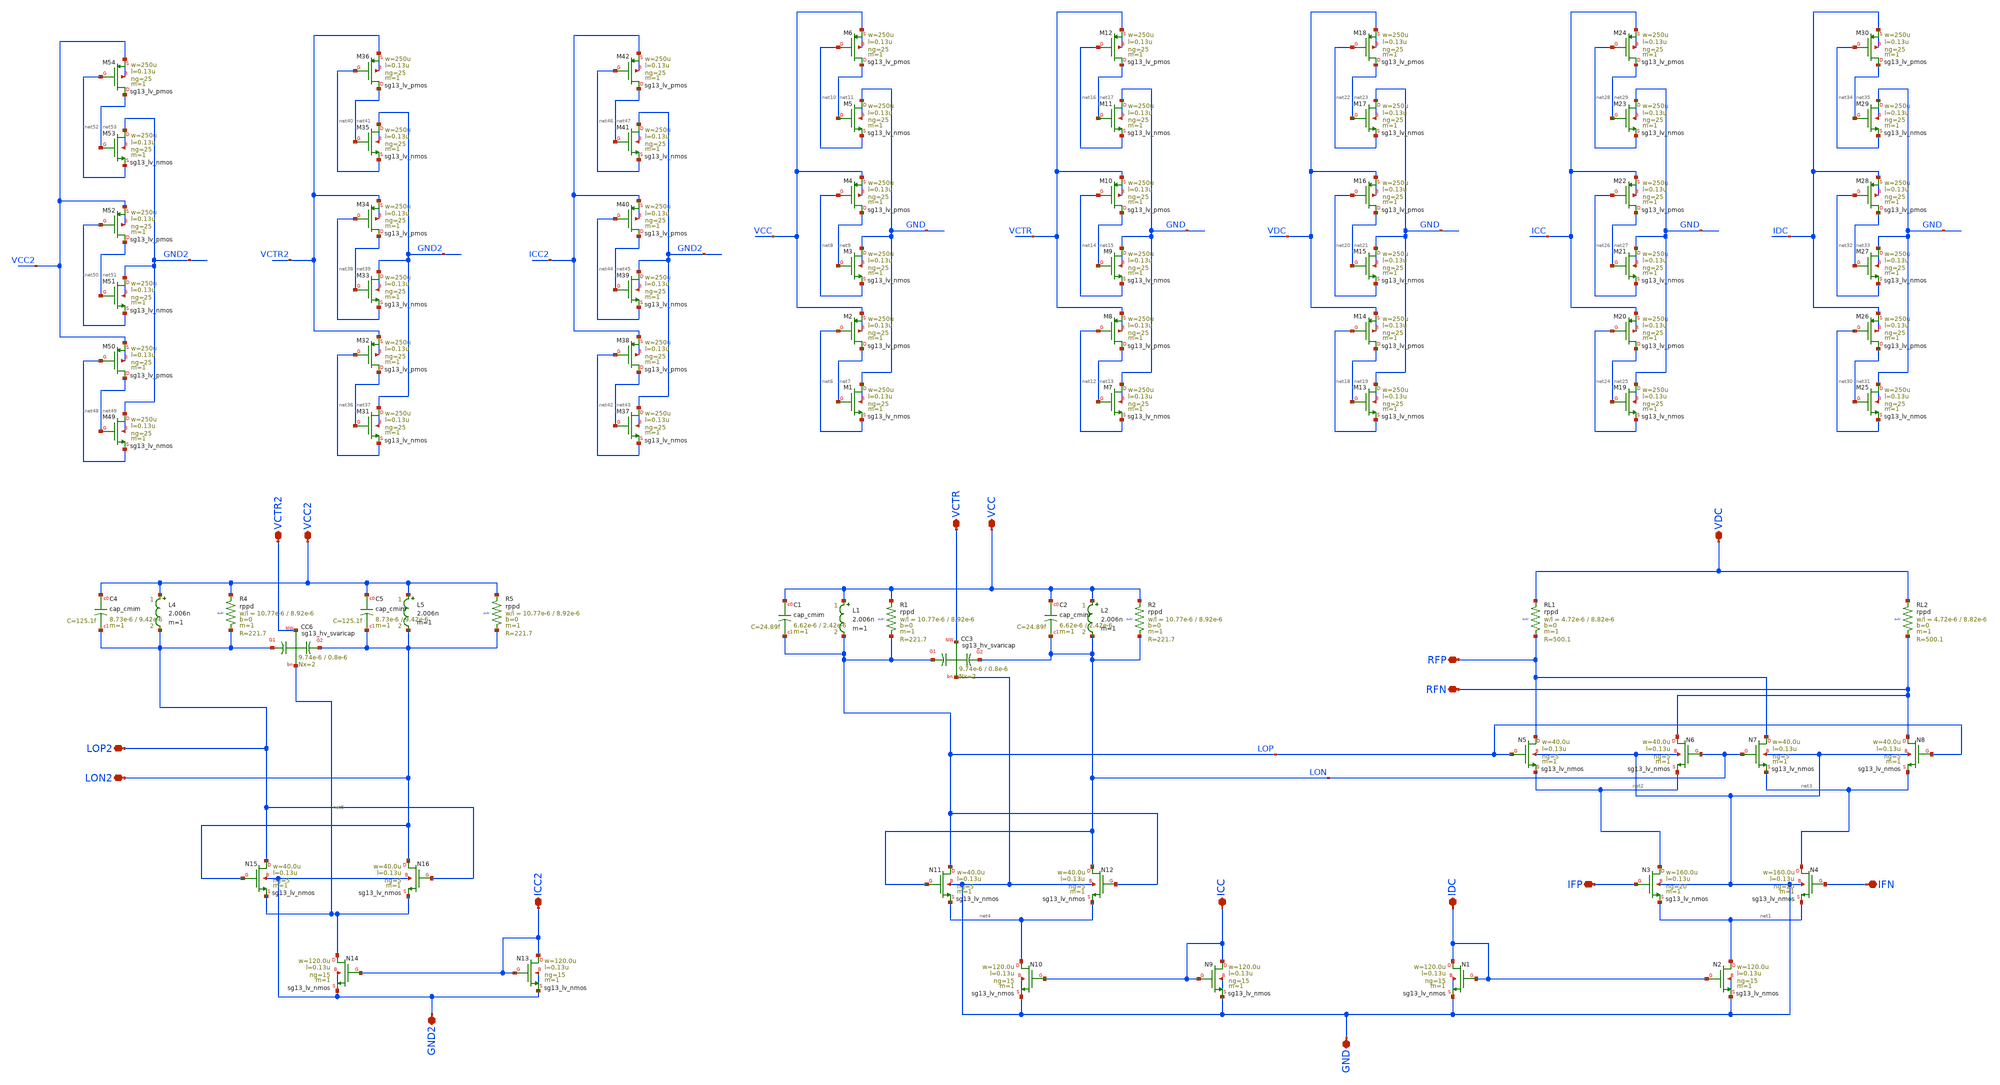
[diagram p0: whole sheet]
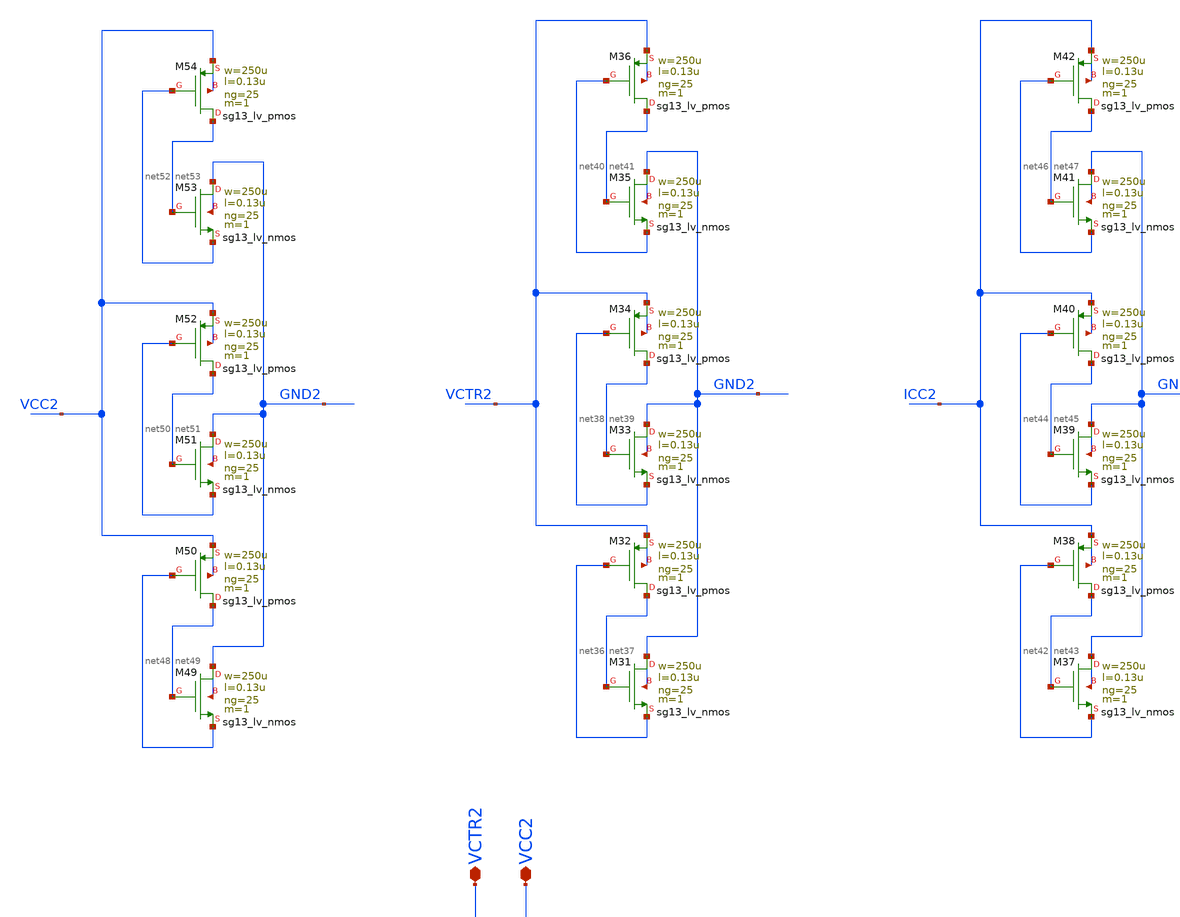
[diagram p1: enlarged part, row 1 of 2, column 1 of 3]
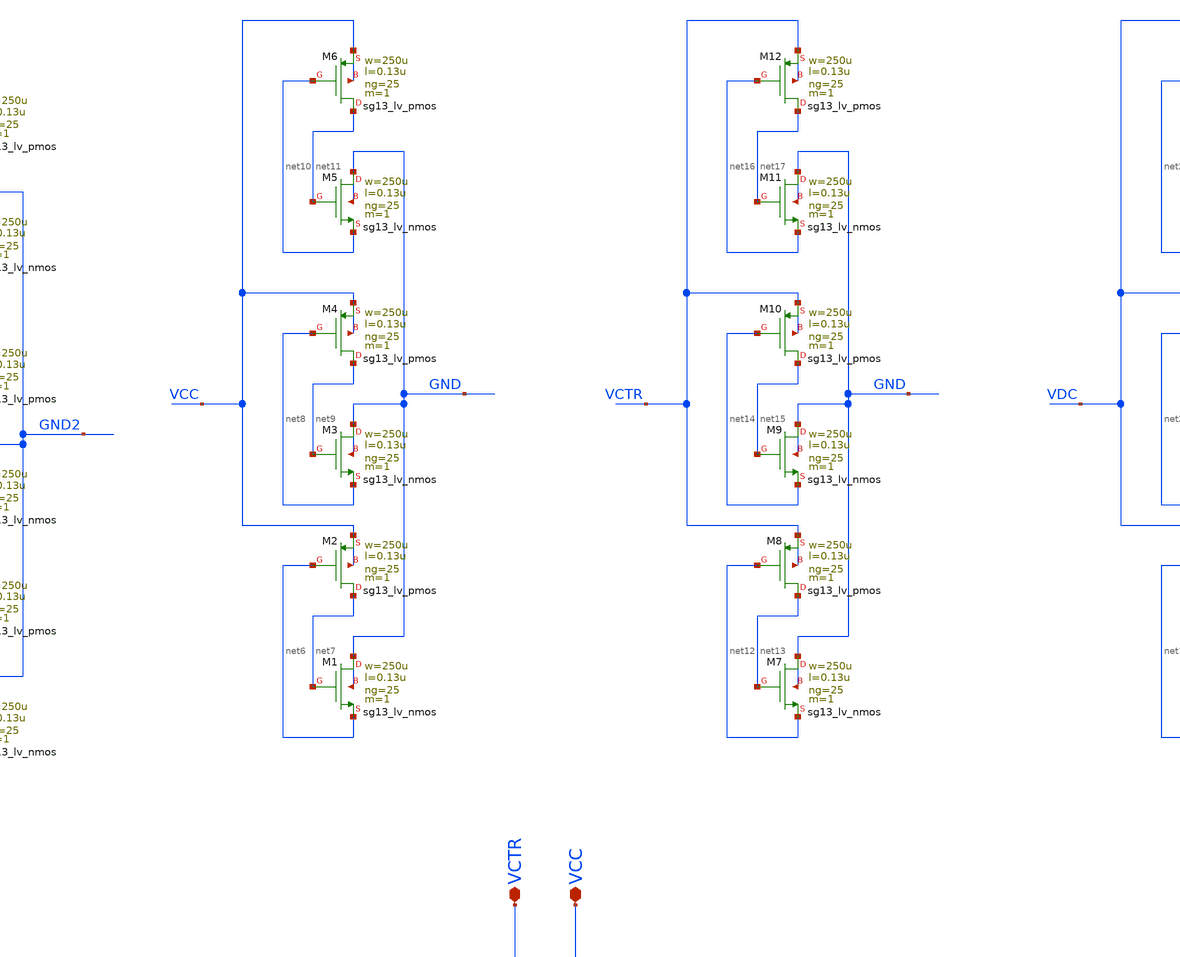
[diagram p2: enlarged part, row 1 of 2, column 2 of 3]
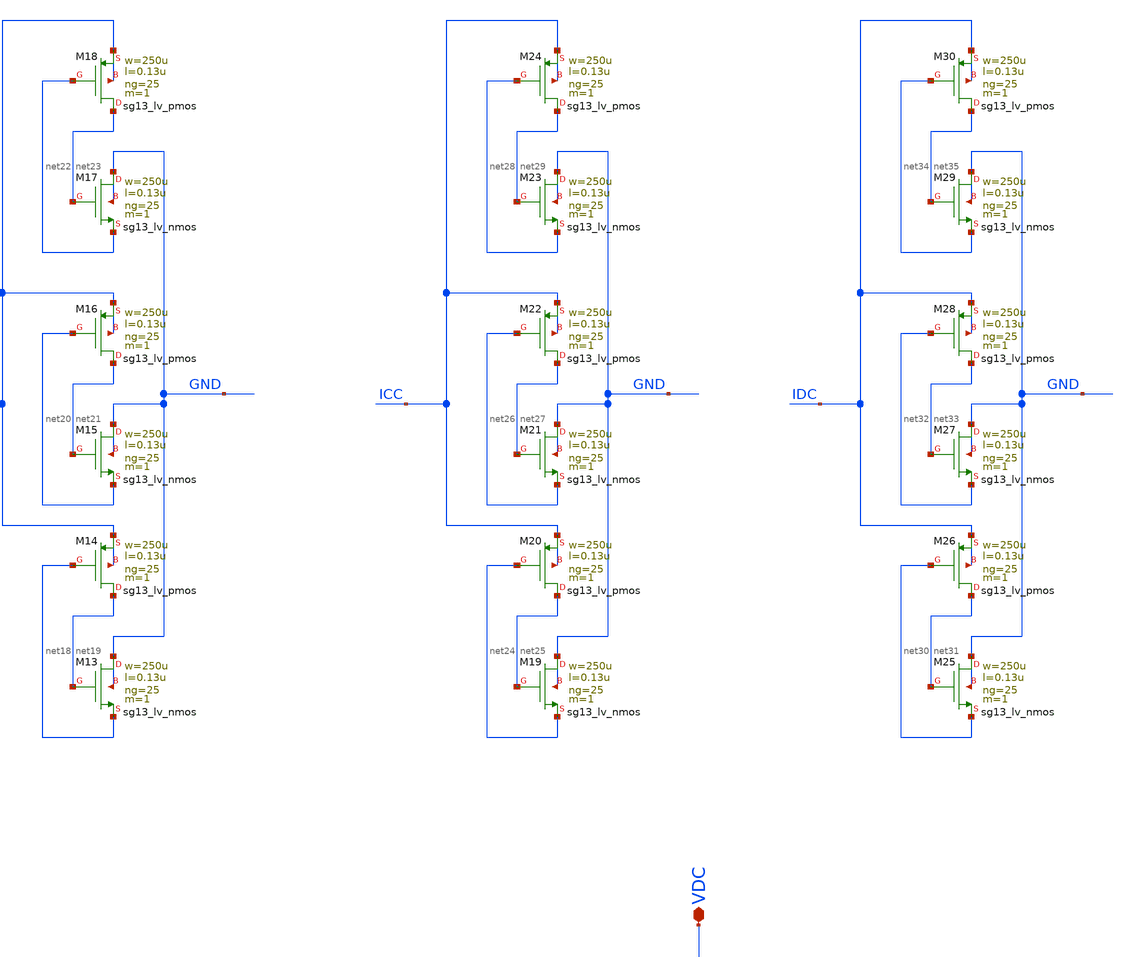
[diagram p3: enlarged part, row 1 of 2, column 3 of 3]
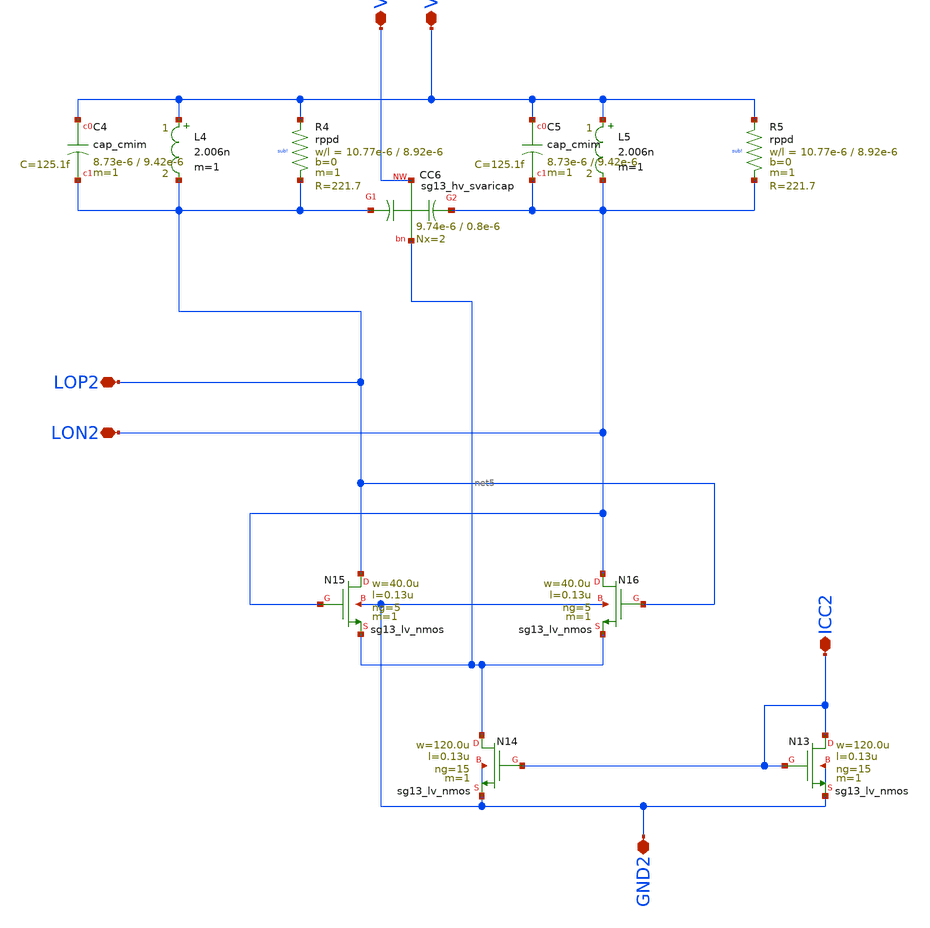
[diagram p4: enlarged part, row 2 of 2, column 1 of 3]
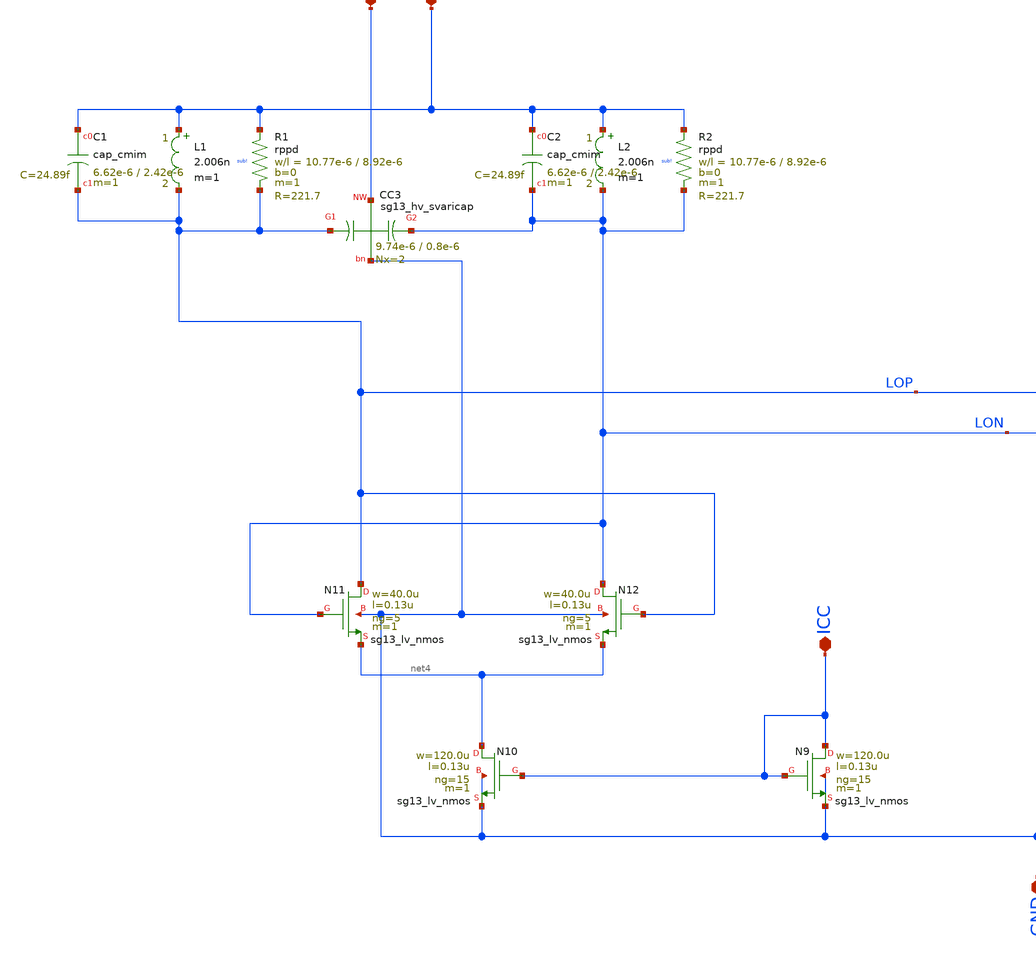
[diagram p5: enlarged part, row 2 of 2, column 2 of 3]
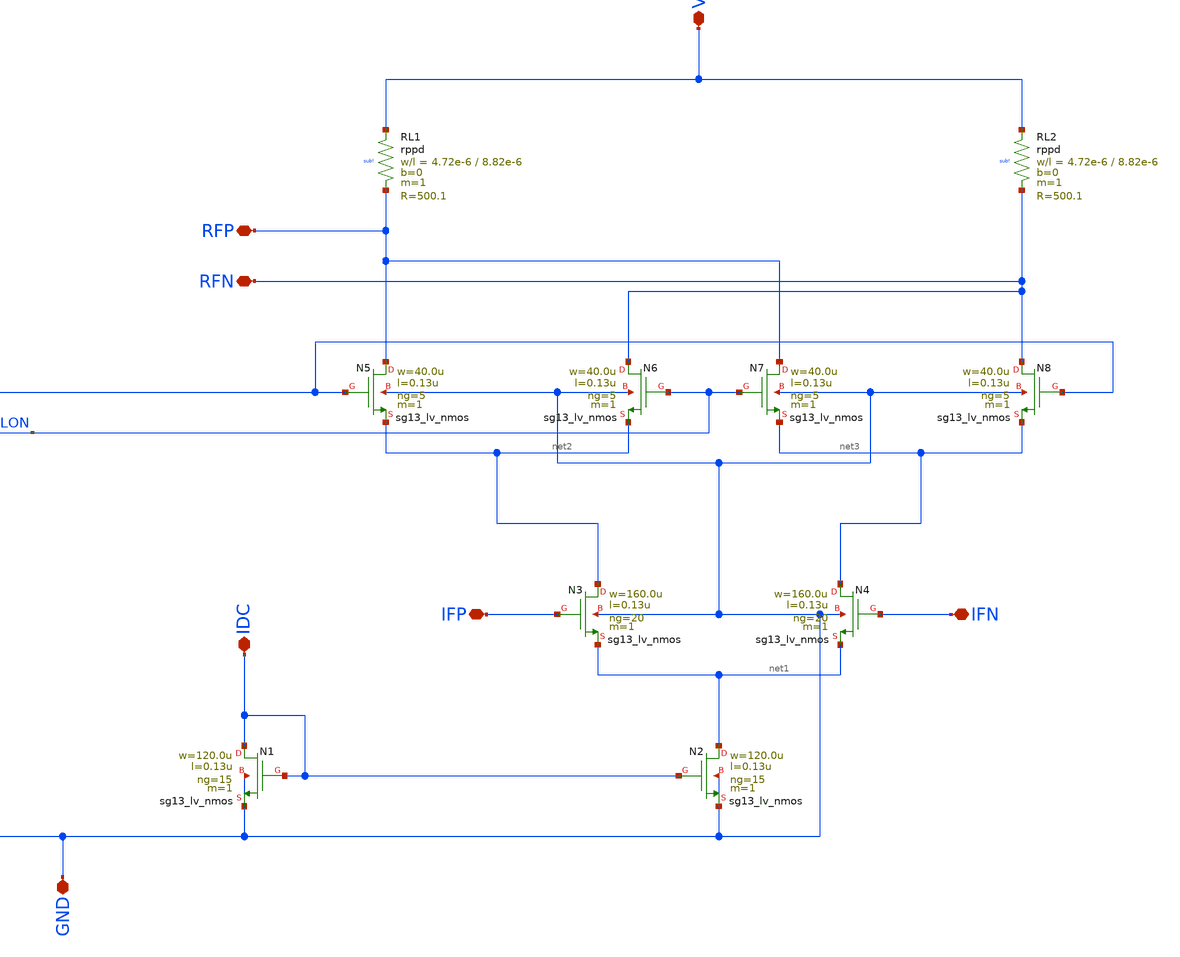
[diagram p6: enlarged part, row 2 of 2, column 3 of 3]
** sch_path: Up_Converter_5GHz/design_data/xschem/FMD_QNC_Up_Converter_5GHz.sch
**.subckt FMD_QNC_Up_Converter_5GHz RFN RFP VDC IFP IFN GND ICC LON2 LOP2 VCC2 ICC2 GND2 IDC VCTR2
*+ VCTR VCC
*.iopin RFN
*.iopin RFP
*.iopin VDC
*.iopin IFP
*.iopin IFN
*.iopin GND
*.iopin ICC
*.iopin LON2
*.iopin LOP2
*.iopin VCC2
*.iopin ICC2
*.iopin GND2
*.iopin IDC
*.iopin VCTR2
*.iopin VCTR
*.iopin VCC
XN6 RFN LON net2 GND sg13_lv_nmos w=40.0u l=0.13u ng=5 m=1 mm_ok=1
XRL2 VDC RFN sub! rppd w=4.72e-6 l=8.82e-6 m=1 b=0 mm_ok=1
XRL1 VDC RFP sub! rppd w=4.72e-6 l=8.82e-6 m=1 b=0 mm_ok=1
XN8 RFN LOP net3 GND sg13_lv_nmos w=40.0u l=0.13u ng=5 m=1 mm_ok=1
XN7 RFP LON net3 GND sg13_lv_nmos w=40.0u l=0.13u ng=5 m=1 mm_ok=1
XN5 RFP LOP net2 GND sg13_lv_nmos w=40.0u l=0.13u ng=5 m=1 mm_ok=1
XN4 net3 IFN net1 GND sg13_lv_nmos w=160.0u l=0.13u ng=20 m=1 mm_ok=1
XN3 net2 IFP net1 GND sg13_lv_nmos w=160.0u l=0.13u ng=20 m=1 mm_ok=1
XN1 IDC IDC GND GND sg13_lv_nmos w=120.0u l=0.13u ng=15 m=1 mm_ok=1
XN2 net1 IDC GND GND sg13_lv_nmos w=120.0u l=0.13u ng=15 m=1 mm_ok=1
XN11 LOP LON net4 GND sg13_lv_nmos w=40.0u l=0.13u ng=5 m=1 mm_ok=1
XN12 LON LOP net4 GND sg13_lv_nmos w=40.0u l=0.13u ng=5 m=1 mm_ok=1
XN9 ICC ICC GND GND sg13_lv_nmos w=120.0u l=0.13u ng=15 m=1 mm_ok=1
XN10 net4 ICC GND GND sg13_lv_nmos w=120.0u l=0.13u ng=15 m=1 mm_ok=1
XC1 VCC LOP cap_cmim w=6.62e-6 l=2.42e-6 m=1 mm_ok=1
XR1 VCC LOP sub! rppd w=10.77e-6 l=8.92e-6 m=1 b=0 mm_ok=1
XC2 VCC LON cap_cmim w=6.62e-6 l=2.42e-6 m=1 mm_ok=1
XR2 VCC LON sub! rppd w=10.77e-6 l=8.92e-6 m=1 b=0 mm_ok=1
XN15 LOP2 LON2 net5 GND2 sg13_lv_nmos w=40.0u l=0.13u ng=5 m=1 mm_ok=1
XN16 LON2 LOP2 net5 GND2 sg13_lv_nmos w=40.0u l=0.13u ng=5 m=1 mm_ok=1
XN13 ICC2 ICC2 GND2 GND2 sg13_lv_nmos w=120.0u l=0.13u ng=15 m=1 mm_ok=1
XN14 net5 ICC2 GND2 GND2 sg13_lv_nmos w=120.0u l=0.13u ng=15 m=1 mm_ok=1
XC4 VCC2 LOP2 cap_cmim w=8.73e-6 l=9.42e-6 m=1 mm_ok=1
XR4 VCC2 LOP2 sub! rppd w=10.77e-6 l=8.92e-6 m=1 b=0 mm_ok=1
XC5 VCC2 LON2 cap_cmim w=8.73e-6 l=9.42e-6 m=1 mm_ok=1
XR5 VCC2 LON2 sub! rppd w=10.77e-6 l=8.92e-6 m=1 b=0 mm_ok=1
L4 VCC2 LOP2 2.006n m=1
L1 VCC LOP 2.006n m=1
L2 VCC LON 2.006n m=1
L5 VCC2 LON2 2.006n m=1
XC6 LOP2 VCTR2 LON2 net5 sg13_hv_svaricap w=9.74e-6 l=0.8e-6 Nx=2
XC3 LOP VCTR LON GND sg13_hv_svaricap w=9.74e-6 l=0.8e-6 Nx=2
XM1 GND net7 net6 GND sg13_lv_nmos w=250u l=0.13u ng=25 m=1 mm_ok=1
XM2 net7 net6 VCC VCC sg13_lv_pmos w=250u l=0.13u ng=25 m=1 mm_ok=1
XM3 GND net9 net8 GND sg13_lv_nmos w=250u l=0.13u ng=25 m=1 mm_ok=1
XM4 net9 net8 VCC VCC sg13_lv_pmos w=250u l=0.13u ng=25 m=1 mm_ok=1
XM5 GND net11 net10 GND sg13_lv_nmos w=250u l=0.13u ng=25 m=1 mm_ok=1
XM6 net11 net10 VCC VCC sg13_lv_pmos w=250u l=0.13u ng=25 m=1 mm_ok=1
XM7 GND net13 net12 GND sg13_lv_nmos w=250u l=0.13u ng=25 m=1 mm_ok=1
XM8 net13 net12 VCTR VCTR sg13_lv_pmos w=250u l=0.13u ng=25 m=1 mm_ok=1
XM9 GND net15 net14 GND sg13_lv_nmos w=250u l=0.13u ng=25 m=1 mm_ok=1
XM10 net15 net14 VCTR VCTR sg13_lv_pmos w=250u l=0.13u ng=25 m=1 mm_ok=1
XM11 GND net17 net16 GND sg13_lv_nmos w=250u l=0.13u ng=25 m=1 mm_ok=1
XM12 net17 net16 VCTR VCTR sg13_lv_pmos w=250u l=0.13u ng=25 m=1 mm_ok=1
XM13 GND net19 net18 GND sg13_lv_nmos w=250u l=0.13u ng=25 m=1 mm_ok=1
XM14 net19 net18 VDC VDC sg13_lv_pmos w=250u l=0.13u ng=25 m=1 mm_ok=1
XM15 GND net21 net20 GND sg13_lv_nmos w=250u l=0.13u ng=25 m=1 mm_ok=1
XM16 net21 net20 VDC VDC sg13_lv_pmos w=250u l=0.13u ng=25 m=1 mm_ok=1
XM17 GND net23 net22 GND sg13_lv_nmos w=250u l=0.13u ng=25 m=1 mm_ok=1
XM18 net23 net22 VDC VDC sg13_lv_pmos w=250u l=0.13u ng=25 m=1 mm_ok=1
XM19 GND net25 net24 GND sg13_lv_nmos w=250u l=0.13u ng=25 m=1 mm_ok=1
XM20 net25 net24 ICC ICC sg13_lv_pmos w=250u l=0.13u ng=25 m=1 mm_ok=1
XM21 GND net27 net26 GND sg13_lv_nmos w=250u l=0.13u ng=25 m=1 mm_ok=1
XM22 net27 net26 ICC ICC sg13_lv_pmos w=250u l=0.13u ng=25 m=1 mm_ok=1
XM23 GND net29 net28 GND sg13_lv_nmos w=250u l=0.13u ng=25 m=1 mm_ok=1
XM24 net29 net28 ICC ICC sg13_lv_pmos w=250u l=0.13u ng=25 m=1 mm_ok=1
XM25 GND net31 net30 GND sg13_lv_nmos w=250u l=0.13u ng=25 m=1 mm_ok=1
XM26 net31 net30 IDC IDC sg13_lv_pmos w=250u l=0.13u ng=25 m=1 mm_ok=1
XM27 GND net33 net32 GND sg13_lv_nmos w=250u l=0.13u ng=25 m=1 mm_ok=1
XM28 net33 net32 IDC IDC sg13_lv_pmos w=250u l=0.13u ng=25 m=1 mm_ok=1
XM29 GND net35 net34 GND sg13_lv_nmos w=250u l=0.13u ng=25 m=1 mm_ok=1
XM30 net35 net34 IDC IDC sg13_lv_pmos w=250u l=0.13u ng=25 m=1 mm_ok=1
XM31 GND2 net37 net36 GND2 sg13_lv_nmos w=250u l=0.13u ng=25 m=1 mm_ok=1
XM32 net37 net36 VCTR2 VCTR2 sg13_lv_pmos w=250u l=0.13u ng=25 m=1 mm_ok=1
XM33 GND2 net39 net38 GND2 sg13_lv_nmos w=250u l=0.13u ng=25 m=1 mm_ok=1
XM34 net39 net38 VCTR2 VCTR2 sg13_lv_pmos w=250u l=0.13u ng=25 m=1 mm_ok=1
XM35 GND2 net41 net40 GND2 sg13_lv_nmos w=250u l=0.13u ng=25 m=1 mm_ok=1
XM36 net41 net40 VCTR2 VCTR2 sg13_lv_pmos w=250u l=0.13u ng=25 m=1 mm_ok=1
XM37 GND2 net43 net42 GND2 sg13_lv_nmos w=250u l=0.13u ng=25 m=1 mm_ok=1
XM38 net43 net42 ICC2 ICC2 sg13_lv_pmos w=250u l=0.13u ng=25 m=1 mm_ok=1
XM39 GND2 net45 net44 GND2 sg13_lv_nmos w=250u l=0.13u ng=25 m=1 mm_ok=1
XM40 net45 net44 ICC2 ICC2 sg13_lv_pmos w=250u l=0.13u ng=25 m=1 mm_ok=1
XM41 GND2 net47 net46 GND2 sg13_lv_nmos w=250u l=0.13u ng=25 m=1 mm_ok=1
XM42 net47 net46 ICC2 ICC2 sg13_lv_pmos w=250u l=0.13u ng=25 m=1 mm_ok=1
XM49 GND2 net49 net48 GND2 sg13_lv_nmos w=250u l=0.13u ng=25 m=1 mm_ok=1
XM50 net49 net48 VCC2 VCC2 sg13_lv_pmos w=250u l=0.13u ng=25 m=1 mm_ok=1
XM51 GND2 net51 net50 GND2 sg13_lv_nmos w=250u l=0.13u ng=25 m=1 mm_ok=1
XM52 net51 net50 VCC2 VCC2 sg13_lv_pmos w=250u l=0.13u ng=25 m=1 mm_ok=1
XM53 GND2 net53 net52 GND2 sg13_lv_nmos w=250u l=0.13u ng=25 m=1 mm_ok=1
XM54 net53 net52 VCC2 VCC2 sg13_lv_pmos w=250u l=0.13u ng=25 m=1 mm_ok=1
**.ends
.end
